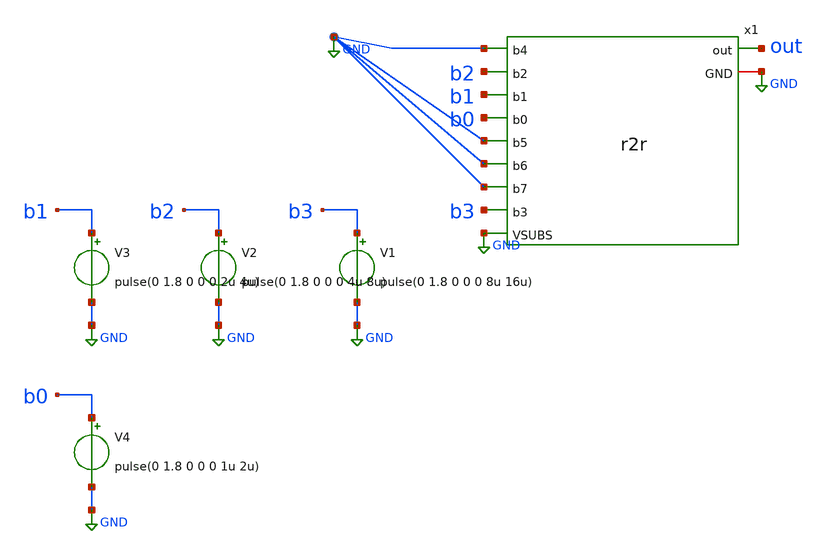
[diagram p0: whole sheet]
** sch_path: xschem/testbench.sch
**.subckt testbench
x1 GND b2 b1 b0 GND GND GND b3 out GND GND r2r
V1 b3 GND pulse(0 1.8 0 0 0 8u 16u)
V2 b2 GND pulse(0 1.8 0 0 0 4u 8u)
V3 b1 GND pulse(0 1.8 0 0 0 2u 4u)
V4 b0 GND pulse(0 1.8 0 0 0 1u 2u)
**** begin user architecture code

.lib $::SKYWATER_MODELS/sky130.lib.spice tt
.tran 1n 20u uic
.save all

**** end user architecture code
**.ends

* expanding   symbol:  r2r.sym # of pins=11
** sym_path: xschem/r2r.sym
** sch_path: xschem/r2r.sch
.subckt r2r b4 b2 b1 b0 b5 b6 b7 b3 out GND VSUBS
*.ipin b0
*.ipin b1
*.ipin b2
*.ipin b3
*.ipin b4
*.ipin b5
*.ipin b6
*.ipin b7
*.opin out
*.ipin VSUBS
*.iopin GND
XR1 net1 b0 VSUBS sky130_fd_pr__res_high_po_0p35 L=40 mult=1 m=1
XR2 net2 b1 VSUBS sky130_fd_pr__res_high_po_0p35 L=40 mult=1 m=1
XR3 net3 b2 VSUBS sky130_fd_pr__res_high_po_0p35 L=40 mult=1 m=1
XR4 net4 b3 VSUBS sky130_fd_pr__res_high_po_0p35 L=40 mult=1 m=1
XR5 net5 b4 VSUBS sky130_fd_pr__res_high_po_0p35 L=40 mult=1 m=1
XR6 net6 b5 VSUBS sky130_fd_pr__res_high_po_0p35 L=40 mult=1 m=1
XR7 net7 b6 VSUBS sky130_fd_pr__res_high_po_0p35 L=40 mult=1 m=1
XR8 out b7 VSUBS sky130_fd_pr__res_high_po_0p35 L=40 mult=1 m=1
XR9 net2 net1 VSUBS sky130_fd_pr__res_high_po_0p35 L=20 mult=1 m=1
XR10 net3 net2 VSUBS sky130_fd_pr__res_high_po_0p35 L=20 mult=1 m=1
XR11 net4 net3 VSUBS sky130_fd_pr__res_high_po_0p35 L=20 mult=1 m=1
XR12 net5 net4 VSUBS sky130_fd_pr__res_high_po_0p35 L=20 mult=1 m=1
XR13 net6 net5 VSUBS sky130_fd_pr__res_high_po_0p35 L=20 mult=1 m=1
XR14 net7 net6 VSUBS sky130_fd_pr__res_high_po_0p35 L=20 mult=1 m=1
XR15 out net7 VSUBS sky130_fd_pr__res_high_po_0p35 L=20 mult=1 m=1
XR16 GND net1 VSUBS sky130_fd_pr__res_high_po_0p35 L=40 mult=1 m=1
.ends

.GLOBAL GND
.end
